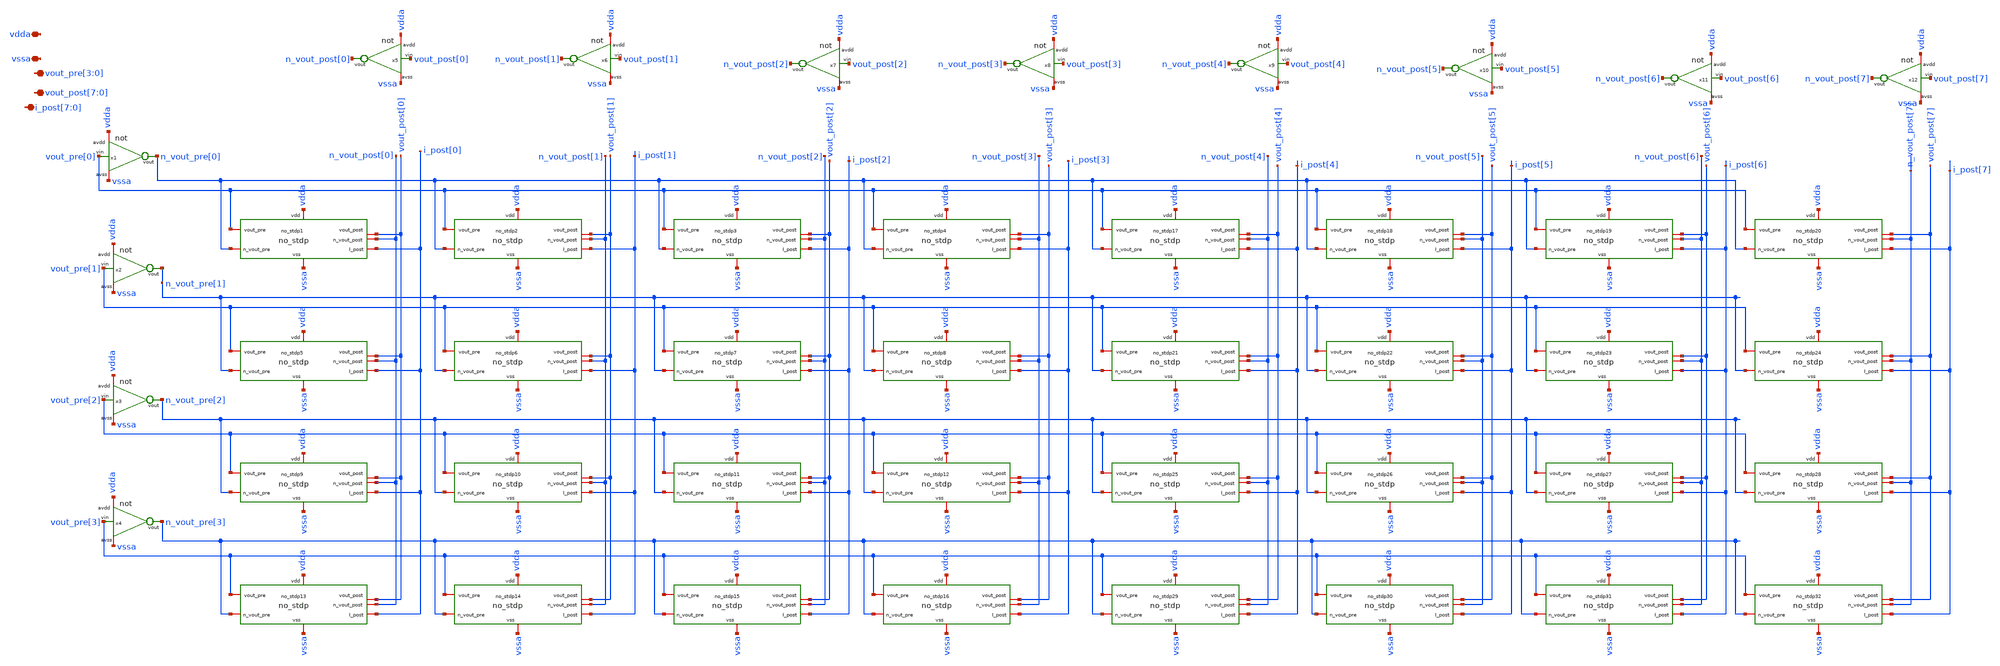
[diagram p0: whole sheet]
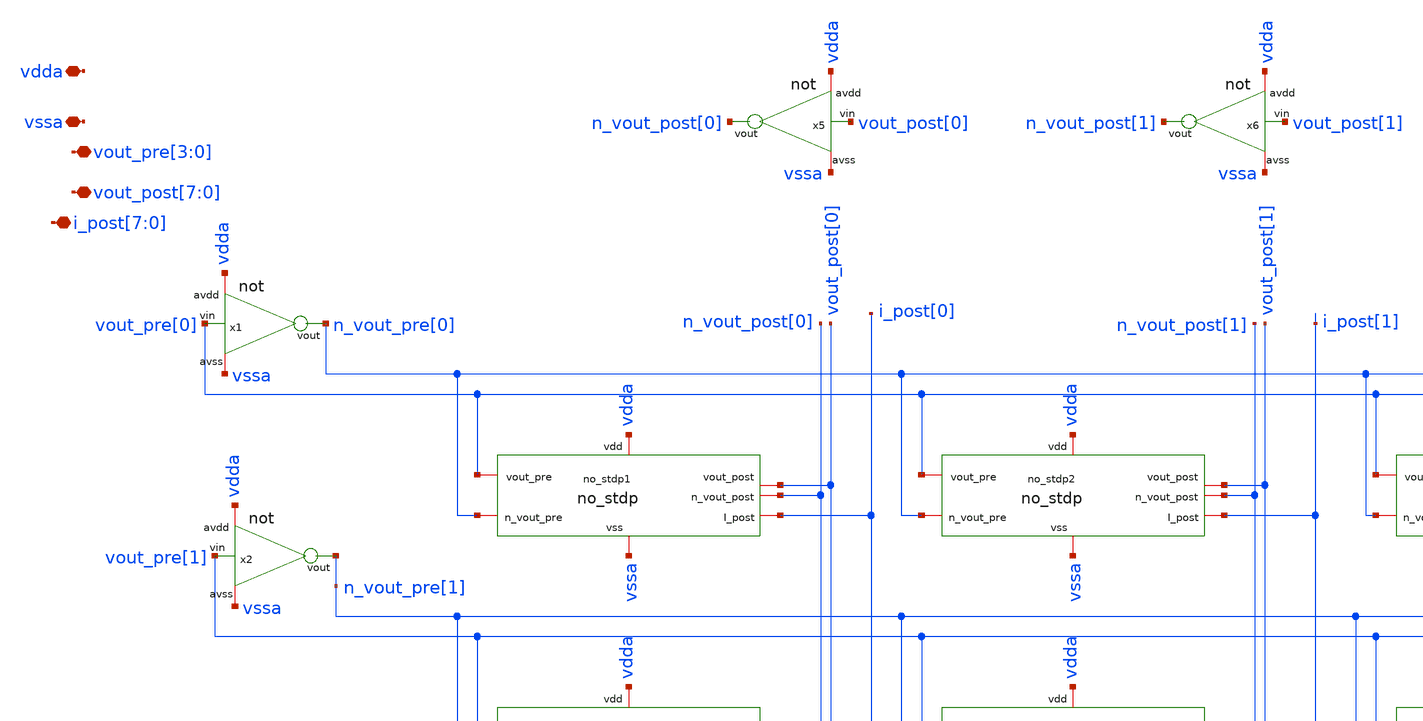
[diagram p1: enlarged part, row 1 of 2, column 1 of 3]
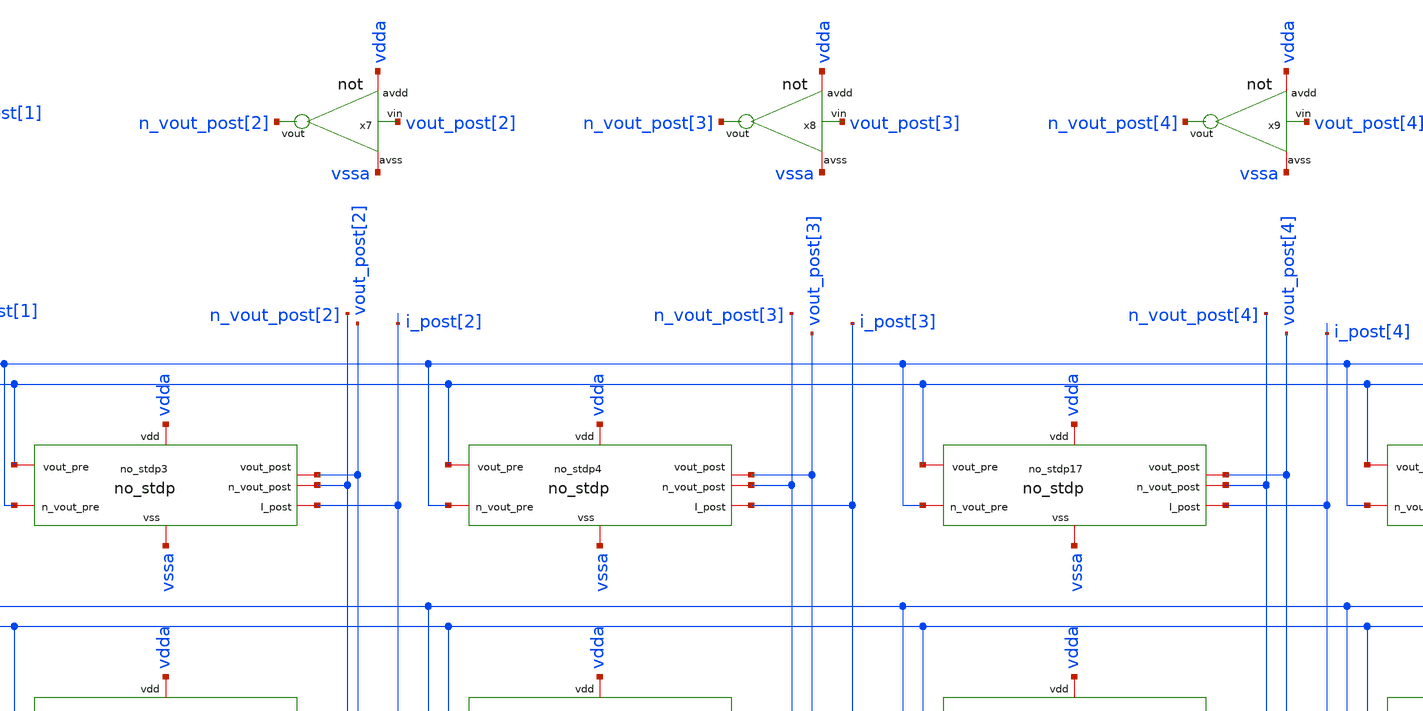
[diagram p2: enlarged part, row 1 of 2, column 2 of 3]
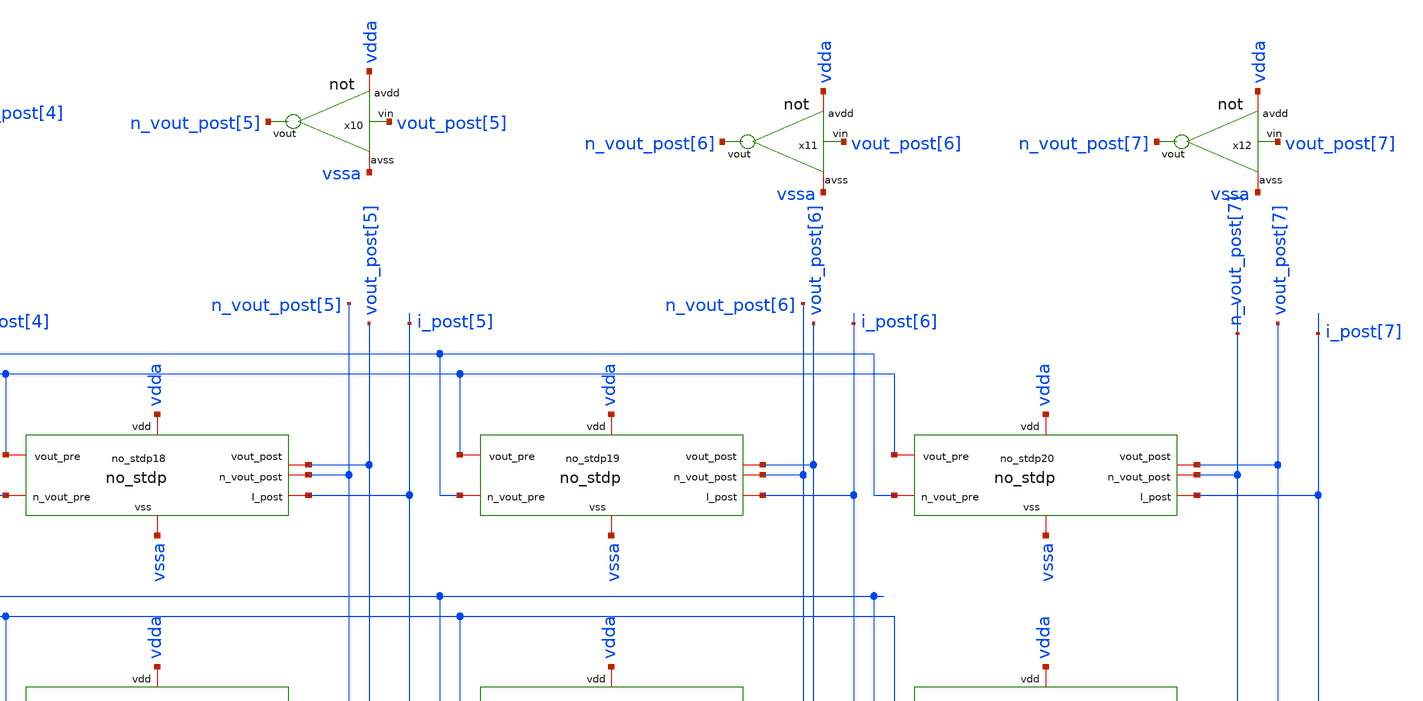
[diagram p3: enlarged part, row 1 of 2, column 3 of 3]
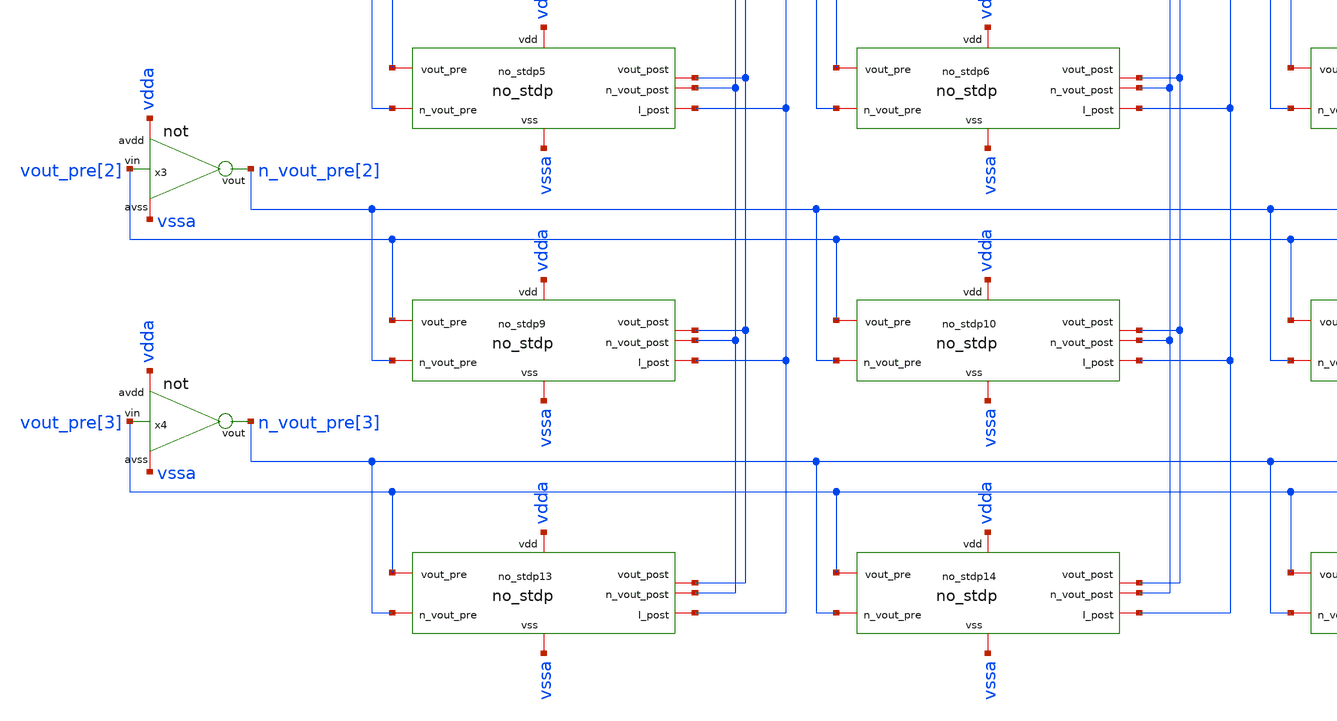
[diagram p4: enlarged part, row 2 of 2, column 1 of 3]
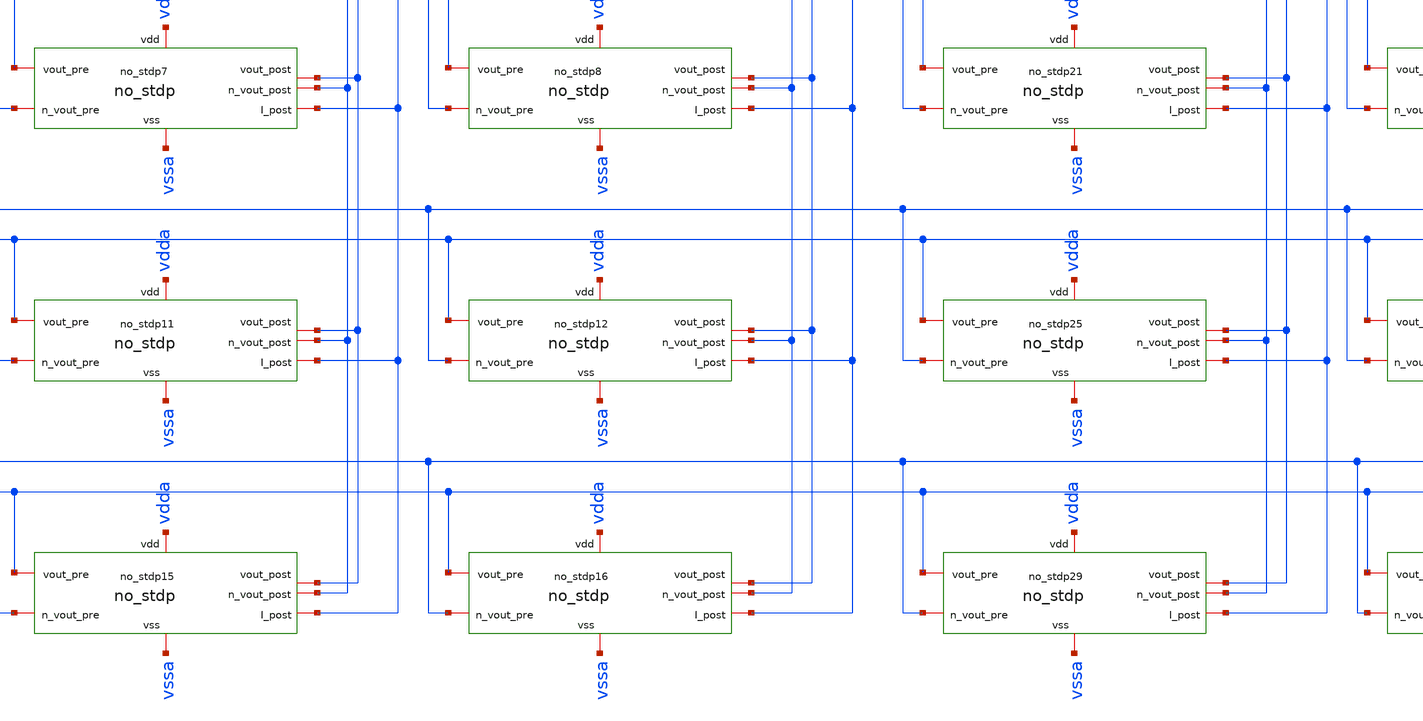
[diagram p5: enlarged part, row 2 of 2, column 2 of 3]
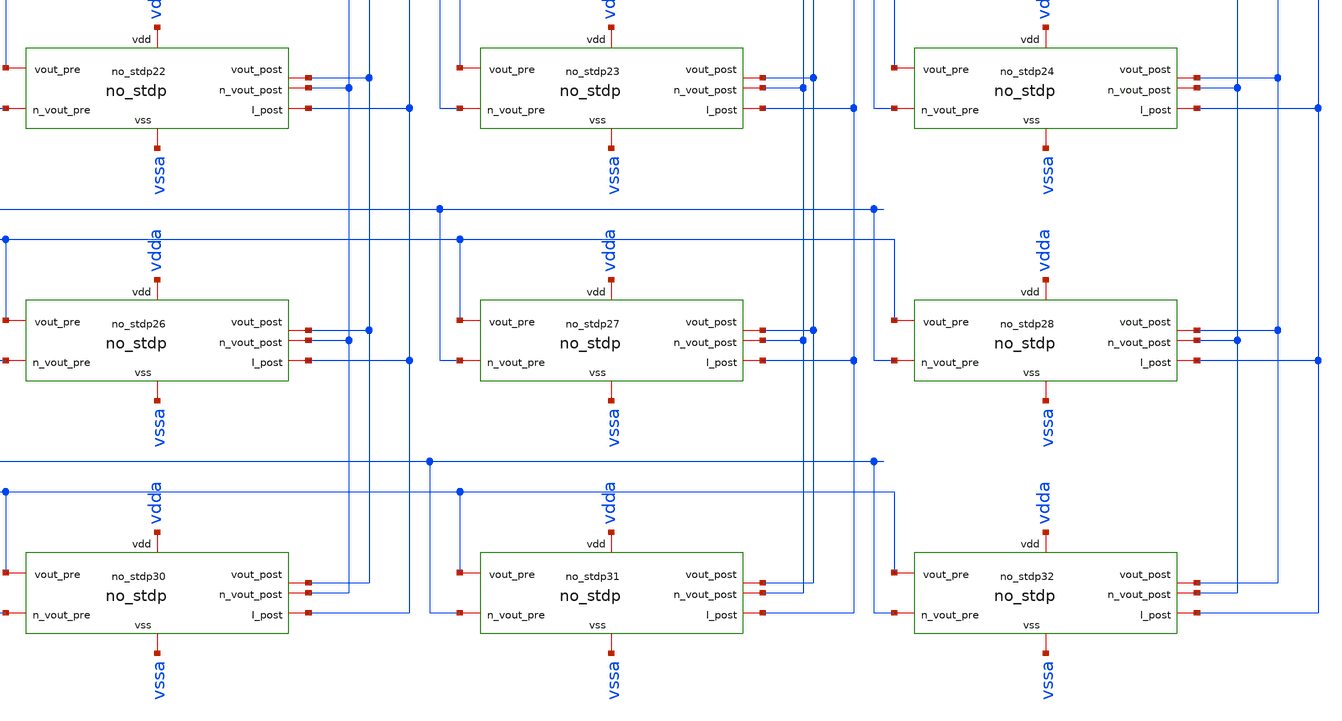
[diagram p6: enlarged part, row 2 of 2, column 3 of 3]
** sch_path: Synapse/no_stdp_4x8.sch
**.subckt no_stdp_4x8 vdda vssa vout_pre[3],vout_pre[2],vout_pre[1],vout_pre[0]
*+ vout_post[7],vout_post[6],vout_post[5],vout_post[4],vout_post[3],vout_post[2],vout_post[1],vout_post[0] i_post[7],i_post[6],i_post[5],i_post[4],i_post[3],i_post[2],i_post[1],i_post[0]
*.iopin vdda
*.iopin vssa
*.iopin vout_pre[3],vout_pre[2],vout_pre[1],vout_pre[0]
*.iopin
*+ vout_post[7],vout_post[6],vout_post[5],vout_post[4],vout_post[3],vout_post[2],vout_post[1],vout_post[0]
*.iopin i_post[7],i_post[6],i_post[5],i_post[4],i_post[3],i_post[2],i_post[1],i_post[0]
xno_stdp1 vdda vssa vout_pre[0] vout_post[0] i_post[0] n_vout_pre[0] n_vout_post[0] no_stdp
xno_stdp2 vdda vssa vout_pre[0] vout_post[1] i_post[1] n_vout_pre[0] n_vout_post[1] no_stdp
xno_stdp3 vdda vssa vout_pre[0] vout_post[2] i_post[2] n_vout_pre[0] n_vout_post[2] no_stdp
xno_stdp4 vdda vssa vout_pre[0] vout_post[3] i_post[3] n_vout_pre[0] n_vout_post[3] no_stdp
xno_stdp5 vdda vssa vout_pre[1] vout_post[0] i_post[0] n_vout_pre[1] n_vout_post[0] no_stdp
xno_stdp6 vdda vssa vout_pre[1] vout_post[1] i_post[1] n_vout_pre[1] n_vout_post[1] no_stdp
xno_stdp7 vdda vssa vout_pre[1] vout_post[2] i_post[2] n_vout_pre[1] n_vout_post[2] no_stdp
xno_stdp8 vdda vssa vout_pre[1] vout_post[3] i_post[3] n_vout_pre[1] n_vout_post[3] no_stdp
xno_stdp9 vdda vssa vout_pre[2] vout_post[0] i_post[0] n_vout_pre[2] n_vout_post[0] no_stdp
xno_stdp10 vdda vssa vout_pre[2] vout_post[1] i_post[1] n_vout_pre[2] n_vout_post[1] no_stdp
xno_stdp11 vdda vssa vout_pre[2] vout_post[2] i_post[2] n_vout_pre[2] n_vout_post[2] no_stdp
xno_stdp12 vdda vssa vout_pre[2] vout_post[3] i_post[3] n_vout_pre[2] n_vout_post[3] no_stdp
xno_stdp13 vdda vssa vout_pre[3] vout_post[0] i_post[0] n_vout_pre[3] n_vout_post[0] no_stdp
xno_stdp14 vdda vssa vout_pre[3] vout_post[1] i_post[1] n_vout_pre[3] n_vout_post[1] no_stdp
xno_stdp15 vdda vssa vout_pre[3] vout_post[2] i_post[2] n_vout_pre[3] n_vout_post[2] no_stdp
xno_stdp16 vdda vssa vout_pre[3] vout_post[3] i_post[3] n_vout_pre[3] n_vout_post[3] no_stdp
xno_stdp17 vdda vssa vout_pre[0] vout_post[4] i_post[4] n_vout_pre[0] n_vout_post[4] no_stdp
xno_stdp18 vdda vssa vout_pre[0] vout_post[5] i_post[5] n_vout_pre[0] n_vout_post[5] no_stdp
xno_stdp19 vdda vssa vout_pre[0] vout_post[6] i_post[6] n_vout_pre[0] n_vout_post[6] no_stdp
xno_stdp20 vdda vssa vout_pre[0] vout_post[7] i_post[7] n_vout_pre[0] n_vout_post[7] no_stdp
xno_stdp21 vdda vssa vout_pre[1] vout_post[4] i_post[4] n_vout_pre[1] n_vout_post[4] no_stdp
xno_stdp22 vdda vssa vout_pre[1] vout_post[5] i_post[5] n_vout_pre[1] n_vout_post[5] no_stdp
xno_stdp23 vdda vssa vout_pre[1] vout_post[6] i_post[6] n_vout_pre[1] n_vout_post[6] no_stdp
xno_stdp24 vdda vssa vout_pre[1] vout_post[7] i_post[7] n_vout_pre[1] n_vout_post[7] no_stdp
xno_stdp25 vdda vssa vout_pre[2] vout_post[4] i_post[4] n_vout_pre[2] n_vout_post[4] no_stdp
xno_stdp26 vdda vssa vout_pre[2] vout_post[5] i_post[5] n_vout_pre[2] n_vout_post[5] no_stdp
xno_stdp27 vdda vssa vout_pre[2] vout_post[6] i_post[6] n_vout_pre[2] n_vout_post[6] no_stdp
xno_stdp28 vdda vssa vout_pre[2] vout_post[7] i_post[7] n_vout_pre[2] n_vout_post[7] no_stdp
xno_stdp29 vdda vssa vout_pre[3] vout_post[4] i_post[4] n_vout_pre[3] n_vout_post[4] no_stdp
xno_stdp30 vdda vssa vout_pre[3] vout_post[5] i_post[5] n_vout_pre[3] n_vout_post[5] no_stdp
xno_stdp31 vdda vssa vout_pre[3] vout_post[6] i_post[6] n_vout_pre[3] n_vout_post[6] no_stdp
xno_stdp32 vdda vssa vout_pre[3] vout_post[7] i_post[7] n_vout_pre[3] n_vout_post[7] no_stdp
x1 vdda vout_pre[0] n_vout_pre[0] vssa not
x2 vdda vout_pre[1] n_vout_pre[1] vssa not
x3 vdda vout_pre[2] n_vout_pre[2] vssa not
x4 vdda vout_pre[3] n_vout_pre[3] vssa not
x5 vdda vout_post[0] n_vout_post[0] vssa not
x6 vdda vout_post[1] n_vout_post[1] vssa not
x7 vdda vout_post[2] n_vout_post[2] vssa not
x8 vdda vout_post[3] n_vout_post[3] vssa not
x9 vdda vout_post[4] n_vout_post[4] vssa not
x10 vdda vout_post[5] n_vout_post[5] vssa not
x11 vdda vout_post[6] n_vout_post[6] vssa not
x12 vdda vout_post[7] n_vout_post[7] vssa not
**.ends
.end
